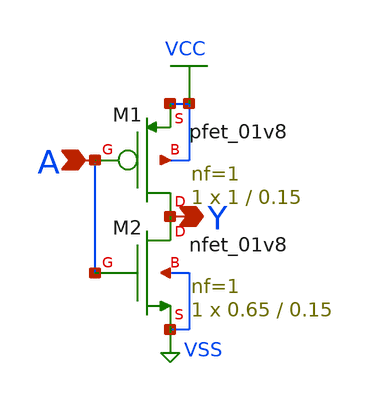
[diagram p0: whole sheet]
** sch_path: elements/not.sch
**.subckt not A Y
*.ipin A
*.opin Y
XM1 Y A VCC VCC sky130_fd_pr__pfet_01v8 L=0.15 W=1 nf=1 ad='int((nf+1)/2) * W/nf * 0.29' as='int((nf+2)/2) * W/nf * 0.29'
+ pd='2*int((nf+1)/2) * (W/nf + 0.29)' ps='2*int((nf+2)/2) * (W/nf + 0.29)' nrd='0.29 / W' nrs='0.29 / W'
+ sa=0 sb=0 sd=0 mult=1 m=1
XM2 Y A VSS VSS sky130_fd_pr__nfet_01v8 L=0.15 W=0.65 nf=1 ad='int((1 + 1)/2) * 0.65 / 1 * 0.29' as='int((1 + 2)/2) * 0.65 / 1 * 0.29'
+ pd='2*int((1 + 1)/2) * (0.65 / 1 + 0.29)' ps='2*int((1 + 2)/2) * (0.65 / 1 + 0.29)' nrd='0.29 / 0.65 '
+ nrs='0.29 / 0.65 ' sa=0 sb=0 sd=0 mult=1 m=1
**.ends
.GLOBAL VCC
.GLOBAL VSS
.end
